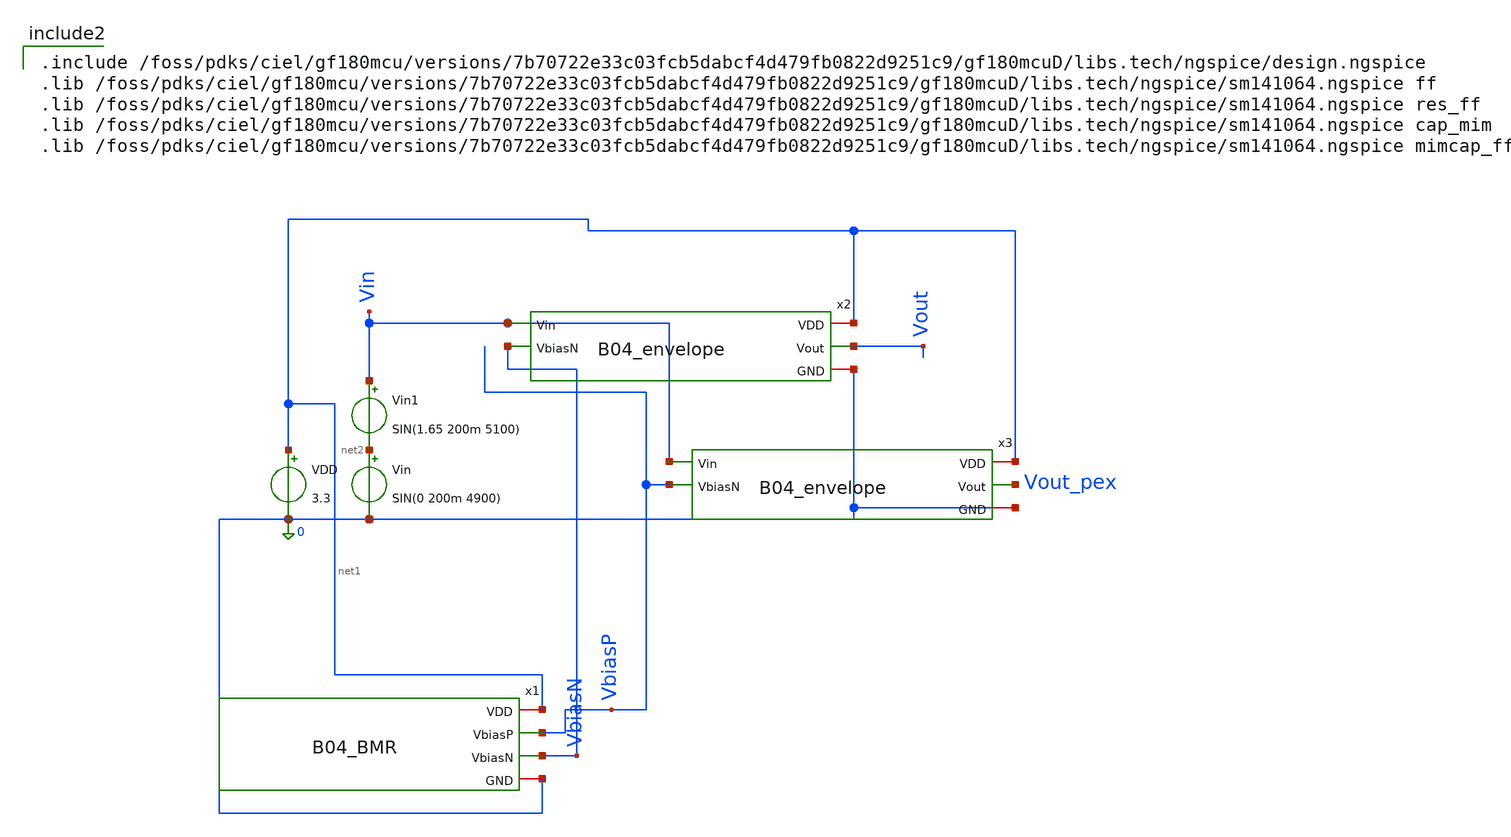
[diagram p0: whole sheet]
** sch_path: analog/B04_tb_envelopev2.sch
**.subckt B04_tb_envelopev2
VDD net1 0 3.3
Vin net2 0 SIN(0 200m 4900)
x1 net1 VbiasP VbiasN 0 B04_BMR
x2 net1 Vin Vout VbiasN 0 B04_envelope
Vin1 Vin net2 SIN(1.65 200m 5100)
x3 net1 Vin Vout_pex VbiasP 0 B04_envelope
**** begin user architecture code


.control
set color0=white
set color1=black
set xbrushwidth=2

echo =================================================
echo TRANSIENT ANALYSIS: ENVELOPE DETECTOR
echo =================================================
* Simulasi dijalankan 20ms untuk melihat 2 bukit penuh dari modulasi 100Hz
tran 10u 20m

* Plot Vin dan Vout di satu layar untuk melihat efek memeluk puncak
plot v(Vin) v(vout) ylabel 'Voltage (V)' xlabel 'Time (s)' title 'Precision Envelope Detector Response'
plot v(VbiasP) v(VbiasN)
plot @m.x2.xm2.m0[id]

.endc



.include /foss/pdks/ciel/gf180mcu/versions/7b70722e33c03fcb5dabcf4d479fb0822d9251c9/gf180mcuD/libs.tech/ngspice/design.ngspice
.lib /foss/pdks/ciel/gf180mcu/versions/7b70722e33c03fcb5dabcf4d479fb0822d9251c9/gf180mcuD/libs.tech/ngspice/sm141064.ngspice ff
.lib /foss/pdks/ciel/gf180mcu/versions/7b70722e33c03fcb5dabcf4d479fb0822d9251c9/gf180mcuD/libs.tech/ngspice/sm141064.ngspice res_ff
.lib /foss/pdks/ciel/gf180mcu/versions/7b70722e33c03fcb5dabcf4d479fb0822d9251c9/gf180mcuD/libs.tech/ngspice/sm141064.ngspice cap_mim
.lib /foss/pdks/ciel/gf180mcu/versions/7b70722e33c03fcb5dabcf4d479fb0822d9251c9/gf180mcuD/libs.tech/ngspice/sm141064.ngspice mimcap_ff

**** end user architecture code
**.ends
.end
